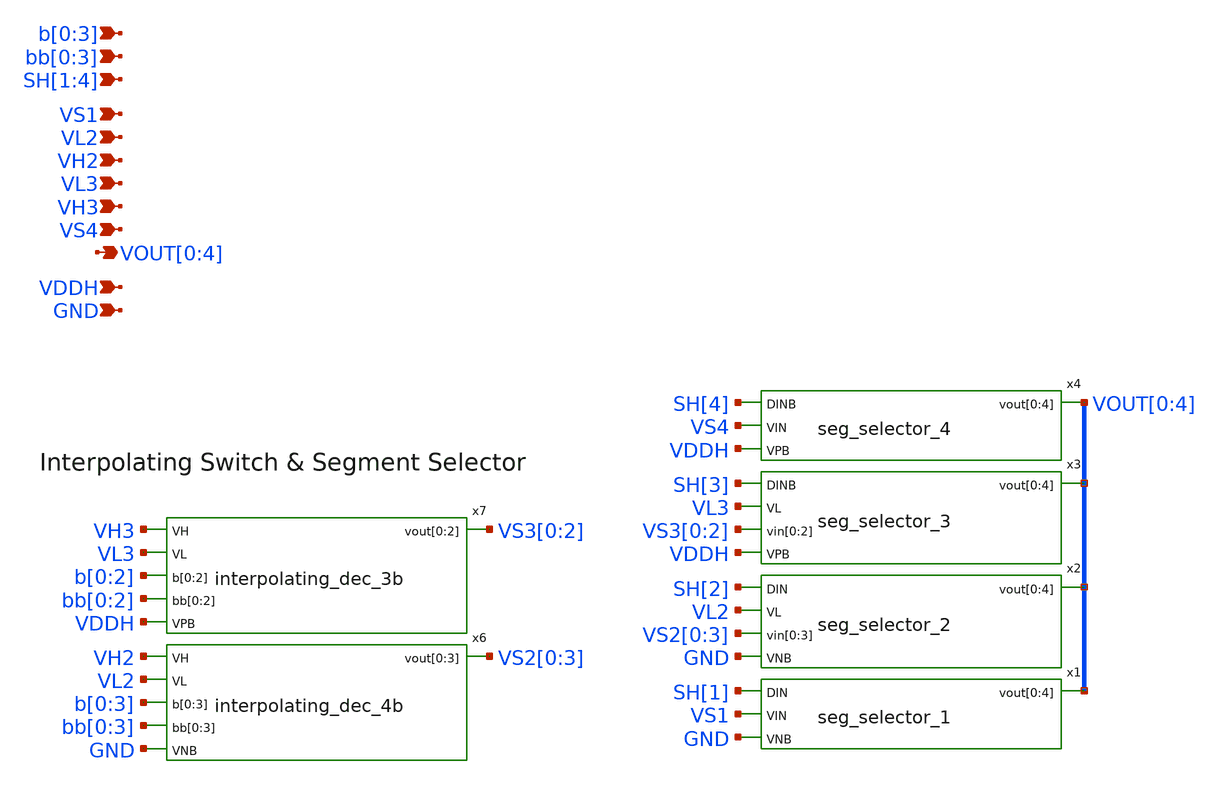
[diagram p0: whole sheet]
** sch_path: xschem/top_final_switch.sch
**.subckt top_final_switch GND VDDH b[0],b[1],b[2],b[3] VOUT[0],VOUT[1],VOUT[2],VOUT[3],VOUT[4]
*+ bb[0],bb[1],bb[2],bb[3] VS1 VH2 VL2 VH3 VL3 VS4 SH[1],SH[2],SH[3],SH[4]
*.ipin GND
*.ipin VDDH
*.ipin b[0],b[1],b[2],b[3]
*.opin VOUT[0],VOUT[1],VOUT[2],VOUT[3],VOUT[4]
*.ipin bb[0],bb[1],bb[2],bb[3]
*.ipin VS1
*.ipin VH2
*.ipin VL2
*.ipin VH3
*.ipin VL3
*.ipin VS4
*.ipin SH[1],SH[2],SH[3],SH[4]
x6 VH2 VL2 b[0] b[1] b[2] b[3] bb[0] bb[1] bb[2] bb[3] VS2[0] VS2[1] VS2[2] VS2[3] GND
+ interpolating_dec_4b
x7 VH3 VL3 b[0] b[1] b[2] bb[0] bb[1] bb[2] VS3[0] VS3[1] VS3[2] VDDH interpolating_dec_3b
x1 SH[1] VS1 VOUT[0] VOUT[1] VOUT[2] VOUT[3] VOUT[4] GND seg_selector_1
x2 SH[2] VL2 VS2[0] VS2[1] VS2[2] VS2[3] VOUT[0] VOUT[1] VOUT[2] VOUT[3] VOUT[4] GND seg_selector_2
x3 SH[3] VL3 VS3[0] VS3[1] VS3[2] VOUT[0] VOUT[1] VOUT[2] VOUT[3] VOUT[4] VDDH seg_selector_3
x4 SH[4] VS4 VOUT[0] VOUT[1] VOUT[2] VOUT[3] VOUT[4] VDDH seg_selector_4
**.ends

* expanding   symbol:  interpolating_dec_4b.sym # of pins=6
** sym_path: xschem/interpolating_dec_4b.sym
** sch_path: xschem/interpolating_dec_4b.sch
.subckt interpolating_dec_4b VH VL b[0] b[1] b[2] b[3] bb[0] bb[1] bb[2] bb[3] vout[0] vout[1]
+ vout[2] vout[3] VNB
*.opin vout[0],vout[1],vout[2],vout[3]
*.ipin VNB
*.ipin b[0],b[1],b[2],b[3]
*.ipin VH
*.ipin VL
*.ipin bb[0],bb[1],bb[2],bb[3]
.param wp=0.42 wn=0.42 l=0.5

XM1 vout[0] b[0] VH VNB sky130_fd_pr__nfet_g5v0d10v5 L=l W=wn nf=1 ad='int((nf+1)/2) * W/nf * 0.29' as='int((nf+2)/2) * W/nf * 0.29'
+ pd='2*int((nf+1)/2) * (W/nf + 0.29)' ps='2*int((nf+2)/2) * (W/nf + 0.29)' nrd='0.29 / W' nrs='0.29 / W'
+ sa=0 sb=0 sd=0 mult=1 m=1
XM2 vout[1] b[1] VH VNB sky130_fd_pr__nfet_g5v0d10v5 L=l W=wn nf=1 ad='int((nf+1)/2) * W/nf * 0.29' as='int((nf+2)/2) * W/nf * 0.29'
+ pd='2*int((nf+1)/2) * (W/nf + 0.29)' ps='2*int((nf+2)/2) * (W/nf + 0.29)' nrd='0.29 / W' nrs='0.29 / W'
+ sa=0 sb=0 sd=0 mult=1 m=1
XM3 vout[2] b[2] VH VNB sky130_fd_pr__nfet_g5v0d10v5 L=l W=wn nf=1 ad='int((nf+1)/2) * W/nf * 0.29' as='int((nf+2)/2) * W/nf * 0.29'
+ pd='2*int((nf+1)/2) * (W/nf + 0.29)' ps='2*int((nf+2)/2) * (W/nf + 0.29)' nrd='0.29 / W' nrs='0.29 / W'
+ sa=0 sb=0 sd=0 mult=1 m=1
XM4 vout[3] b[3] VH VNB sky130_fd_pr__nfet_g5v0d10v5 L=l W=wn nf=1 ad='int((nf+1)/2) * W/nf * 0.29' as='int((nf+2)/2) * W/nf * 0.29'
+ pd='2*int((nf+1)/2) * (W/nf + 0.29)' ps='2*int((nf+2)/2) * (W/nf + 0.29)' nrd='0.29 / W' nrs='0.29 / W'
+ sa=0 sb=0 sd=0 mult=1 m=1
XM5 vout[0] bb[0] VL VNB sky130_fd_pr__nfet_g5v0d10v5 L=l W=wn nf=1 ad='int((nf+1)/2) * W/nf * 0.29'
+ as='int((nf+2)/2) * W/nf * 0.29' pd='2*int((nf+1)/2) * (W/nf + 0.29)' ps='2*int((nf+2)/2) * (W/nf + 0.29)'
+ nrd='0.29 / W' nrs='0.29 / W' sa=0 sb=0 sd=0 mult=1 m=1
XM6 vout[1] bb[1] VL VNB sky130_fd_pr__nfet_g5v0d10v5 L=l W=wn nf=1 ad='int((nf+1)/2) * W/nf * 0.29'
+ as='int((nf+2)/2) * W/nf * 0.29' pd='2*int((nf+1)/2) * (W/nf + 0.29)' ps='2*int((nf+2)/2) * (W/nf + 0.29)'
+ nrd='0.29 / W' nrs='0.29 / W' sa=0 sb=0 sd=0 mult=1 m=1
XM7 vout[2] bb[2] VL VNB sky130_fd_pr__nfet_g5v0d10v5 L=l W=wn nf=1 ad='int((nf+1)/2) * W/nf * 0.29'
+ as='int((nf+2)/2) * W/nf * 0.29' pd='2*int((nf+1)/2) * (W/nf + 0.29)' ps='2*int((nf+2)/2) * (W/nf + 0.29)'
+ nrd='0.29 / W' nrs='0.29 / W' sa=0 sb=0 sd=0 mult=1 m=1
XM8 vout[3] bb[3] VL VNB sky130_fd_pr__nfet_g5v0d10v5 L=l W=wn nf=1 ad='int((nf+1)/2) * W/nf * 0.29'
+ as='int((nf+2)/2) * W/nf * 0.29' pd='2*int((nf+1)/2) * (W/nf + 0.29)' ps='2*int((nf+2)/2) * (W/nf + 0.29)'
+ nrd='0.29 / W' nrs='0.29 / W' sa=0 sb=0 sd=0 mult=1 m=1
.ends


* expanding   symbol:  interpolating_dec_3b.sym # of pins=6
** sym_path: xschem/interpolating_dec_3b.sym
** sch_path: xschem/interpolating_dec_3b.sch
.subckt interpolating_dec_3b VH VL b[0] b[1] b[2] bb[0] bb[1] bb[2] vout[0] vout[1] vout[2] VPB
*.opin vout[0],vout[1],vout[2]
*.ipin b[0],b[1],b[2]
*.ipin VPB
*.ipin VH
*.ipin VL
*.ipin bb[0],bb[1],bb[2]
.param wp=0.42 wn=0.42 l=0.5

XM5 vout[0] b[0] VL VPB sky130_fd_pr__pfet_g5v0d10v5 L=l W=wp nf=1 ad='int((nf+1)/2) * W/nf * 0.29' as='int((nf+2)/2) * W/nf * 0.29'
+ pd='2*int((nf+1)/2) * (W/nf + 0.29)' ps='2*int((nf+2)/2) * (W/nf + 0.29)' nrd='0.29 / W' nrs='0.29 / W'
+ sa=0 sb=0 sd=0 mult=1 m=1
XM6 vout[1] b[1] VL VPB sky130_fd_pr__pfet_g5v0d10v5 L=l W=wp nf=1 ad='int((nf+1)/2) * W/nf * 0.29' as='int((nf+2)/2) * W/nf * 0.29'
+ pd='2*int((nf+1)/2) * (W/nf + 0.29)' ps='2*int((nf+2)/2) * (W/nf + 0.29)' nrd='0.29 / W' nrs='0.29 / W'
+ sa=0 sb=0 sd=0 mult=1 m=1
XM7 vout[2] b[2] VL VPB sky130_fd_pr__pfet_g5v0d10v5 L=l W=wp nf=1 ad='int((nf+1)/2) * W/nf * 0.29' as='int((nf+2)/2) * W/nf * 0.29'
+ pd='2*int((nf+1)/2) * (W/nf + 0.29)' ps='2*int((nf+2)/2) * (W/nf + 0.29)' nrd='0.29 / W' nrs='0.29 / W'
+ sa=0 sb=0 sd=0 mult=1 m=1
XM1 vout[0] bb[0] VH VPB sky130_fd_pr__pfet_g5v0d10v5 L=l W=wp nf=1 ad='int((nf+1)/2) * W/nf * 0.29'
+ as='int((nf+2)/2) * W/nf * 0.29' pd='2*int((nf+1)/2) * (W/nf + 0.29)' ps='2*int((nf+2)/2) * (W/nf + 0.29)'
+ nrd='0.29 / W' nrs='0.29 / W' sa=0 sb=0 sd=0 mult=1 m=1
XM2 vout[1] bb[1] VH VPB sky130_fd_pr__pfet_g5v0d10v5 L=l W=wp nf=1 ad='int((nf+1)/2) * W/nf * 0.29'
+ as='int((nf+2)/2) * W/nf * 0.29' pd='2*int((nf+1)/2) * (W/nf + 0.29)' ps='2*int((nf+2)/2) * (W/nf + 0.29)'
+ nrd='0.29 / W' nrs='0.29 / W' sa=0 sb=0 sd=0 mult=1 m=1
XM3 vout[2] bb[2] VH VPB sky130_fd_pr__pfet_g5v0d10v5 L=l W=wp nf=1 ad='int((nf+1)/2) * W/nf * 0.29'
+ as='int((nf+2)/2) * W/nf * 0.29' pd='2*int((nf+1)/2) * (W/nf + 0.29)' ps='2*int((nf+2)/2) * (W/nf + 0.29)'
+ nrd='0.29 / W' nrs='0.29 / W' sa=0 sb=0 sd=0 mult=1 m=1
.ends


* expanding   symbol:  seg_selector_1.sym # of pins=4
** sym_path: xschem/seg_selector_1.sym
** sch_path: xschem/seg_selector_1.sch
.subckt seg_selector_1 DIN VIN vout[0] vout[1] vout[2] vout[3] vout[4] VNB
*.opin vout[0],vout[1],vout[2],vout[3],vout[4]
*.ipin VNB
*.ipin DIN
*.ipin VIN
.param wp=0.42 wn=0.42 l=0.5

XM1 vout[0] DIN VIN VNB sky130_fd_pr__nfet_g5v0d10v5 L=l W=wn nf=1 ad='int((nf+1)/2) * W/nf * 0.29' as='int((nf+2)/2) * W/nf * 0.29'
+ pd='2*int((nf+1)/2) * (W/nf + 0.29)' ps='2*int((nf+2)/2) * (W/nf + 0.29)' nrd='0.29 / W' nrs='0.29 / W'
+ sa=0 sb=0 sd=0 mult=1 m=1
XM2 vout[1] DIN VIN VNB sky130_fd_pr__nfet_g5v0d10v5 L=l W=wn nf=1 ad='int((nf+1)/2) * W/nf * 0.29' as='int((nf+2)/2) * W/nf * 0.29'
+ pd='2*int((nf+1)/2) * (W/nf + 0.29)' ps='2*int((nf+2)/2) * (W/nf + 0.29)' nrd='0.29 / W' nrs='0.29 / W'
+ sa=0 sb=0 sd=0 mult=1 m=1
XM3 vout[2] DIN VIN VNB sky130_fd_pr__nfet_g5v0d10v5 L=l W=wn nf=1 ad='int((nf+1)/2) * W/nf * 0.29' as='int((nf+2)/2) * W/nf * 0.29'
+ pd='2*int((nf+1)/2) * (W/nf + 0.29)' ps='2*int((nf+2)/2) * (W/nf + 0.29)' nrd='0.29 / W' nrs='0.29 / W'
+ sa=0 sb=0 sd=0 mult=1 m=1
XM4 vout[3] DIN VIN VNB sky130_fd_pr__nfet_g5v0d10v5 L=l W=wn nf=1 ad='int((nf+1)/2) * W/nf * 0.29' as='int((nf+2)/2) * W/nf * 0.29'
+ pd='2*int((nf+1)/2) * (W/nf + 0.29)' ps='2*int((nf+2)/2) * (W/nf + 0.29)' nrd='0.29 / W' nrs='0.29 / W'
+ sa=0 sb=0 sd=0 mult=1 m=1
XM5 vout[4] DIN VIN VNB sky130_fd_pr__nfet_g5v0d10v5 L=l W=wn nf=1 ad='int((nf+1)/2) * W/nf * 0.29' as='int((nf+2)/2) * W/nf * 0.29'
+ pd='2*int((nf+1)/2) * (W/nf + 0.29)' ps='2*int((nf+2)/2) * (W/nf + 0.29)' nrd='0.29 / W' nrs='0.29 / W'
+ sa=0 sb=0 sd=0 mult=1 m=1
.ends


* expanding   symbol:  seg_selector_2.sym # of pins=5
** sym_path: xschem/seg_selector_2.sym
** sch_path: xschem/seg_selector_2.sch
.subckt seg_selector_2 DIN VL vin[0] vin[1] vin[2] vin[3] vout[0] vout[1] vout[2] vout[3] vout[4]
+ VNB
*.opin vout[0],vout[1],vout[2],vout[3],vout[4]
*.ipin VNB
*.ipin DIN
*.ipin vin[0],vin[1],vin[2],vin[3]
*.ipin VL
.param wp=0.42 wn=0.42 l=0.5

XM1 vout[0] DIN VL VNB sky130_fd_pr__nfet_g5v0d10v5 L=l W=wn nf=1 ad='int((nf+1)/2) * W/nf * 0.29' as='int((nf+2)/2) * W/nf * 0.29'
+ pd='2*int((nf+1)/2) * (W/nf + 0.29)' ps='2*int((nf+2)/2) * (W/nf + 0.29)' nrd='0.29 / W' nrs='0.29 / W'
+ sa=0 sb=0 sd=0 mult=1 m=1
XM2 vout[1] DIN vin[0] VNB sky130_fd_pr__nfet_g5v0d10v5 L=l W=wn nf=1 ad='int((nf+1)/2) * W/nf * 0.29'
+ as='int((nf+2)/2) * W/nf * 0.29' pd='2*int((nf+1)/2) * (W/nf + 0.29)' ps='2*int((nf+2)/2) * (W/nf + 0.29)'
+ nrd='0.29 / W' nrs='0.29 / W' sa=0 sb=0 sd=0 mult=1 m=1
XM3 vout[2] DIN vin[1] VNB sky130_fd_pr__nfet_g5v0d10v5 L=l W=wn nf=1 ad='int((nf+1)/2) * W/nf * 0.29'
+ as='int((nf+2)/2) * W/nf * 0.29' pd='2*int((nf+1)/2) * (W/nf + 0.29)' ps='2*int((nf+2)/2) * (W/nf + 0.29)'
+ nrd='0.29 / W' nrs='0.29 / W' sa=0 sb=0 sd=0 mult=1 m=1
XM4 vout[3] DIN vin[2] VNB sky130_fd_pr__nfet_g5v0d10v5 L=l W=wn nf=1 ad='int((nf+1)/2) * W/nf * 0.29'
+ as='int((nf+2)/2) * W/nf * 0.29' pd='2*int((nf+1)/2) * (W/nf + 0.29)' ps='2*int((nf+2)/2) * (W/nf + 0.29)'
+ nrd='0.29 / W' nrs='0.29 / W' sa=0 sb=0 sd=0 mult=1 m=1
XM5 vout[4] DIN vin[3] VNB sky130_fd_pr__nfet_g5v0d10v5 L=l W=wn nf=1 ad='int((nf+1)/2) * W/nf * 0.29'
+ as='int((nf+2)/2) * W/nf * 0.29' pd='2*int((nf+1)/2) * (W/nf + 0.29)' ps='2*int((nf+2)/2) * (W/nf + 0.29)'
+ nrd='0.29 / W' nrs='0.29 / W' sa=0 sb=0 sd=0 mult=1 m=1
.ends


* expanding   symbol:  seg_selector_3.sym # of pins=5
** sym_path: xschem/seg_selector_3.sym
** sch_path: xschem/seg_selector_3.sch
.subckt seg_selector_3 DINB VL vin[0] vin[1] vin[2] vout[0] vout[1] vout[2] vout[3] vout[4] VPB
*.opin vout[0],vout[1],vout[2],vout[3],vout[4]
*.ipin VPB
*.ipin DINB
*.ipin vin[0],vin[1],vin[2]
*.ipin VL
.param wp=0.42 wn=0.42 l=0.5

XM1 vout[0] DINB VL VPB sky130_fd_pr__pfet_g5v0d10v5 L=l W=wp nf=1 ad='int((nf+1)/2) * W/nf * 0.29' as='int((nf+2)/2) * W/nf * 0.29'
+ pd='2*int((nf+1)/2) * (W/nf + 0.29)' ps='2*int((nf+2)/2) * (W/nf + 0.29)' nrd='0.29 / W' nrs='0.29 / W'
+ sa=0 sb=0 sd=0 mult=1 m=1
XM2 vout[1] DINB VL VPB sky130_fd_pr__pfet_g5v0d10v5 L=l W=wp nf=1 ad='int((nf+1)/2) * W/nf * 0.29' as='int((nf+2)/2) * W/nf * 0.29'
+ pd='2*int((nf+1)/2) * (W/nf + 0.29)' ps='2*int((nf+2)/2) * (W/nf + 0.29)' nrd='0.29 / W' nrs='0.29 / W'
+ sa=0 sb=0 sd=0 mult=1 m=1
XM3 vout[2] DINB vin[0] VPB sky130_fd_pr__pfet_g5v0d10v5 L=l W=wp nf=1 ad='int((nf+1)/2) * W/nf * 0.29'
+ as='int((nf+2)/2) * W/nf * 0.29' pd='2*int((nf+1)/2) * (W/nf + 0.29)' ps='2*int((nf+2)/2) * (W/nf + 0.29)'
+ nrd='0.29 / W' nrs='0.29 / W' sa=0 sb=0 sd=0 mult=1 m=1
XM4 vout[3] DINB vin[1] VPB sky130_fd_pr__pfet_g5v0d10v5 L=l W=wp nf=1 ad='int((nf+1)/2) * W/nf * 0.29'
+ as='int((nf+2)/2) * W/nf * 0.29' pd='2*int((nf+1)/2) * (W/nf + 0.29)' ps='2*int((nf+2)/2) * (W/nf + 0.29)'
+ nrd='0.29 / W' nrs='0.29 / W' sa=0 sb=0 sd=0 mult=1 m=1
XM5 vout[4] DINB vin[2] VPB sky130_fd_pr__pfet_g5v0d10v5 L=l W=wp nf=1 ad='int((nf+1)/2) * W/nf * 0.29'
+ as='int((nf+2)/2) * W/nf * 0.29' pd='2*int((nf+1)/2) * (W/nf + 0.29)' ps='2*int((nf+2)/2) * (W/nf + 0.29)'
+ nrd='0.29 / W' nrs='0.29 / W' sa=0 sb=0 sd=0 mult=1 m=1
.ends


* expanding   symbol:  seg_selector_4.sym # of pins=4
** sym_path: xschem/seg_selector_4.sym
** sch_path: xschem/seg_selector_4.sch
.subckt seg_selector_4 DINB VIN vout[0] vout[1] vout[2] vout[3] vout[4] VPB
*.opin vout[0],vout[1],vout[2],vout[3],vout[4]
*.ipin VPB
*.ipin DINB
*.ipin VIN
.param wp=0.42 wn=0.42 l=0.5

XM1 vout[0] DINB VIN VPB sky130_fd_pr__pfet_g5v0d10v5 L=l W=wp nf=1 ad='int((nf+1)/2) * W/nf * 0.29'
+ as='int((nf+2)/2) * W/nf * 0.29' pd='2*int((nf+1)/2) * (W/nf + 0.29)' ps='2*int((nf+2)/2) * (W/nf + 0.29)'
+ nrd='0.29 / W' nrs='0.29 / W' sa=0 sb=0 sd=0 mult=1 m=1
XM2 vout[1] DINB VIN VPB sky130_fd_pr__pfet_g5v0d10v5 L=l W=wp nf=1 ad='int((nf+1)/2) * W/nf * 0.29'
+ as='int((nf+2)/2) * W/nf * 0.29' pd='2*int((nf+1)/2) * (W/nf + 0.29)' ps='2*int((nf+2)/2) * (W/nf + 0.29)'
+ nrd='0.29 / W' nrs='0.29 / W' sa=0 sb=0 sd=0 mult=1 m=1
XM3 vout[2] DINB VIN VPB sky130_fd_pr__pfet_g5v0d10v5 L=l W=wp nf=1 ad='int((nf+1)/2) * W/nf * 0.29'
+ as='int((nf+2)/2) * W/nf * 0.29' pd='2*int((nf+1)/2) * (W/nf + 0.29)' ps='2*int((nf+2)/2) * (W/nf + 0.29)'
+ nrd='0.29 / W' nrs='0.29 / W' sa=0 sb=0 sd=0 mult=1 m=1
XM4 vout[3] DINB VIN VPB sky130_fd_pr__pfet_g5v0d10v5 L=l W=wp nf=1 ad='int((nf+1)/2) * W/nf * 0.29'
+ as='int((nf+2)/2) * W/nf * 0.29' pd='2*int((nf+1)/2) * (W/nf + 0.29)' ps='2*int((nf+2)/2) * (W/nf + 0.29)'
+ nrd='0.29 / W' nrs='0.29 / W' sa=0 sb=0 sd=0 mult=1 m=1
XM5 vout[4] DINB VIN VPB sky130_fd_pr__pfet_g5v0d10v5 L=l W=wp nf=1 ad='int((nf+1)/2) * W/nf * 0.29'
+ as='int((nf+2)/2) * W/nf * 0.29' pd='2*int((nf+1)/2) * (W/nf + 0.29)' ps='2*int((nf+2)/2) * (W/nf + 0.29)'
+ nrd='0.29 / W' nrs='0.29 / W' sa=0 sb=0 sd=0 mult=1 m=1
.ends

.end
